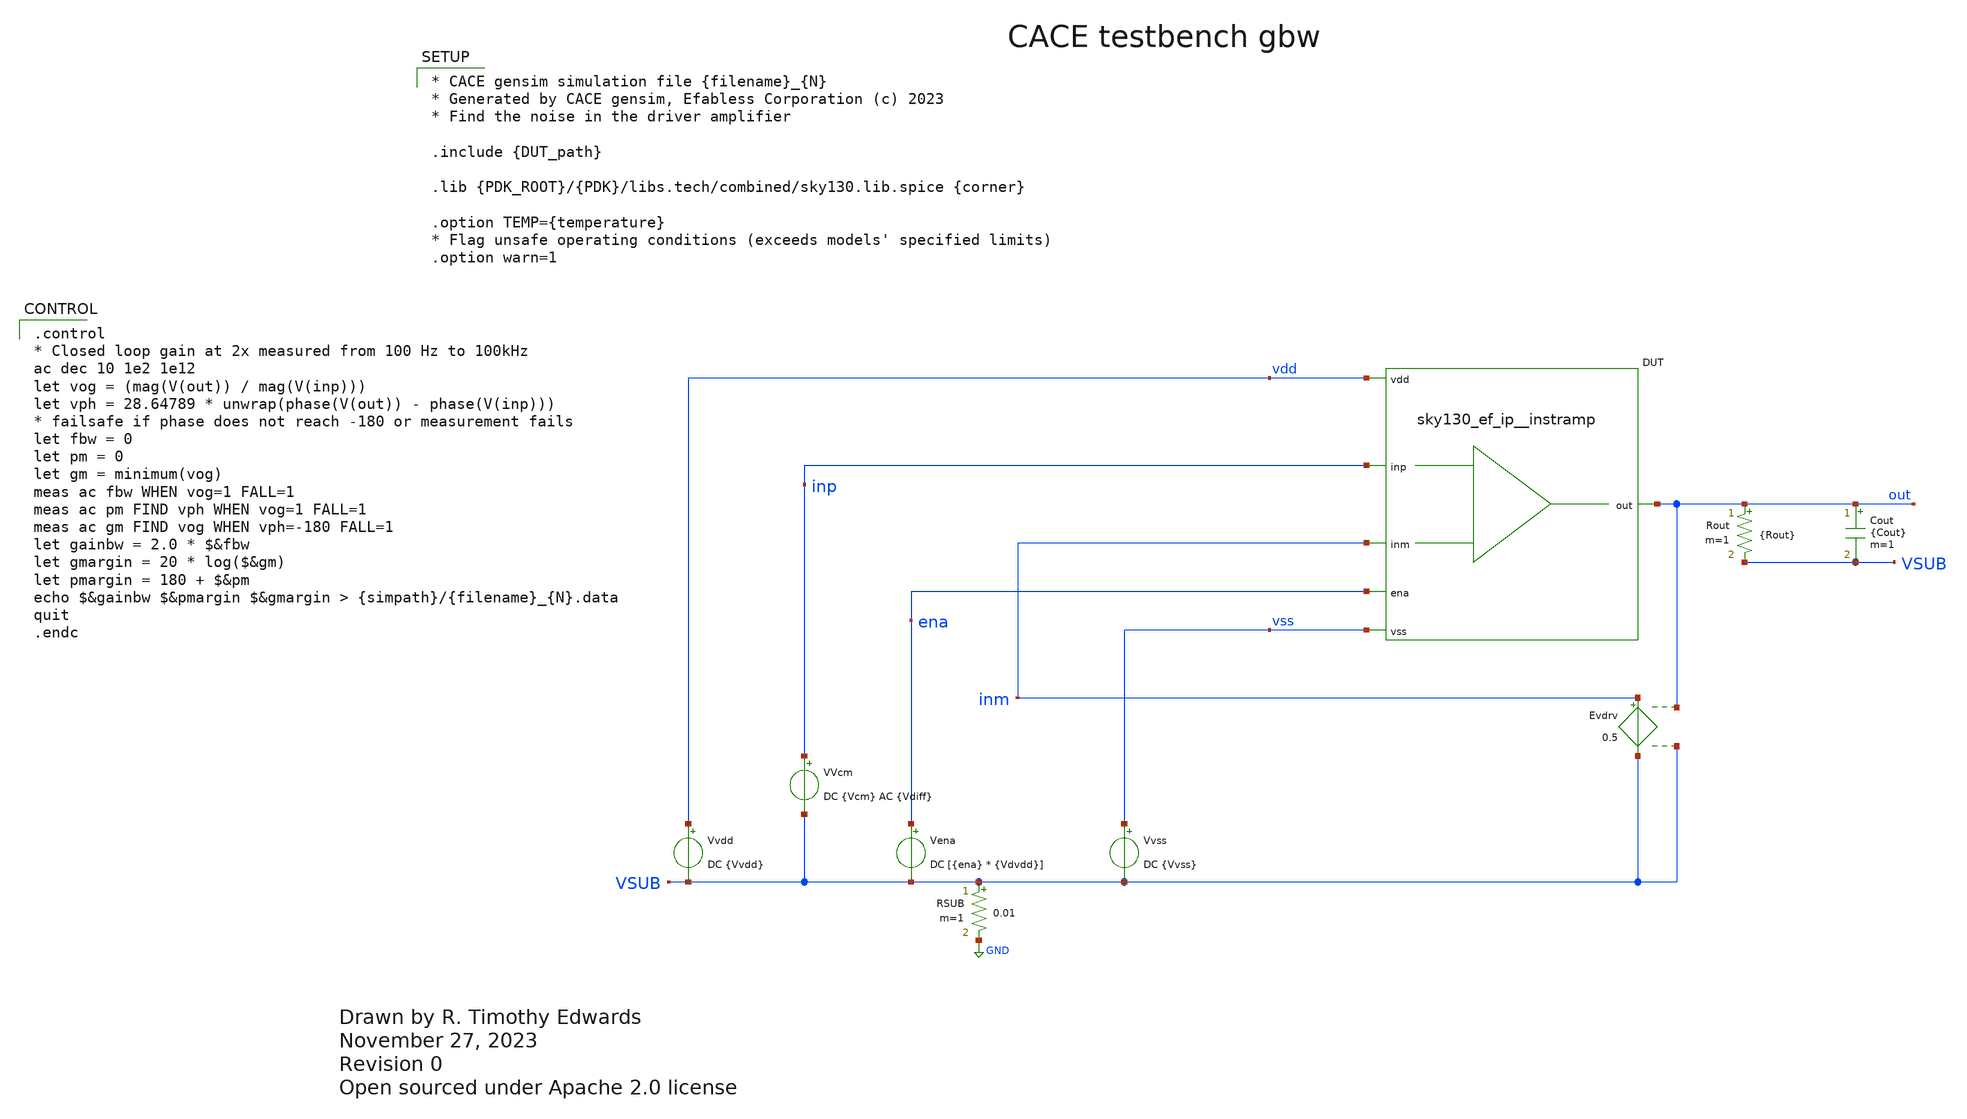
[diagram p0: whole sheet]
** sch_path: cace/gbw.sch
* Open sourced under Apache 2.0 license
**.subckt gbw
VVcm inp VSUB DC {Vcm} AC {Vdiff}
Vena ena VSUB DC [{ena} * {Vdvdd}]
Vvss vss VSUB DC {Vvss}
Rout out VSUB {Rout} m=1
Cout out VSUB {Cout} m=1
Vvdd vdd VSUB DC {Vvdd}
RSUB VSUB GND 0.01 m=1
XDUT {PIN|vdd|vdd} {PIN|vss|vss} {PIN|inm|inm} {PIN|inp|inp} {PIN|out|out} {PIN|ena|ena} {DUT_name}
Evdrv inm VSUB out VSUB 0.5
**** begin user architecture code

.control
* Closed loop gain at 2x measured from 100 Hz to 100kHz
ac dec 10 1e2 1e12
let vog = (mag(V(out)) / mag(V(inp)))
let vph = 28.64789 * unwrap(phase(V(out)) - phase(V(inp)))
* failsafe if phase does not reach -180 or measurement fails
let fbw = 0
let pm = 0
let gm = minimum(vog)
meas ac fbw WHEN vog=1 FALL=1
meas ac pm FIND vph WHEN vog=1 FALL=1
meas ac gm FIND vog WHEN vph=-180 FALL=1
let gainbw = 2.0 * $&fbw
let gmargin = 20 * log($&gm)
let pmargin = 180 + $&pm
echo $&gainbw $&pmargin $&gmargin > {simpath}/{filename}_{N}.data
quit
.endc



* CACE gensim simulation file {filename}_{N}
* Generated by CACE gensim, Efabless Corporation (c) 2023
* Find the noise in the driver amplifier

.include {DUT_path}

.lib {PDK_ROOT}/{PDK}/libs.tech/combined/sky130.lib.spice {corner}

.option TEMP={temperature}
* Flag unsafe operating conditions (exceeds models' specified limits)
.option warn=1


**** end user architecture code
**.ends
.GLOBAL GND
.end
